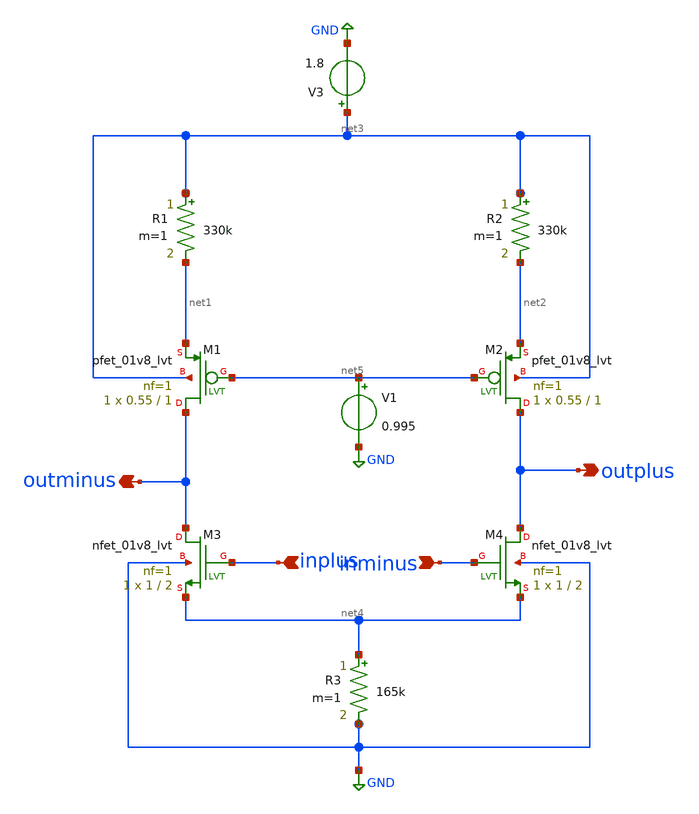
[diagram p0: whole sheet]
** sch_path: botopamp.sch
**.subckt botopamp inplus outminus outplus inminus
*.ipin inplus
*.opin outminus
*.opin outplus
*.ipin inminus
XM1 outminus net5 net1 net3 sky130_fd_pr__pfet_01v8_lvt L=1 W=0.55 nf=1 ad='int((nf+1)/2) * W/nf * 0.29'
+ as='int((nf+2)/2) * W/nf * 0.29' pd='2*int((nf+1)/2) * (W/nf + 0.29)' ps='2*int((nf+2)/2) * (W/nf + 0.29)'
+ nrd='0.29 / W' nrs='0.29 / W' sa=0 sb=0 sd=0 mult=1 m=1
XM2 outplus net5 net2 net3 sky130_fd_pr__pfet_01v8_lvt L=1 W=0.55 nf=1 ad='int((nf+1)/2) * W/nf * 0.29'
+ as='int((nf+2)/2) * W/nf * 0.29' pd='2*int((nf+1)/2) * (W/nf + 0.29)' ps='2*int((nf+2)/2) * (W/nf + 0.29)'
+ nrd='0.29 / W' nrs='0.29 / W' sa=0 sb=0 sd=0 mult=1 m=1
XM3 outminus inplus net4 GND sky130_fd_pr__nfet_01v8_lvt L=2 W=1 nf=1 ad='int((nf+1)/2) * W/nf * 0.29'
+ as='int((nf+2)/2) * W/nf * 0.29' pd='2*int((nf+1)/2) * (W/nf + 0.29)' ps='2*int((nf+2)/2) * (W/nf + 0.29)'
+ nrd='0.29 / W' nrs='0.29 / W' sa=0 sb=0 sd=0 mult=1 m=1
XM4 outplus inminus net4 GND sky130_fd_pr__nfet_01v8_lvt L=2 W=1 nf=1 ad='int((nf+1)/2) * W/nf * 0.29'
+ as='int((nf+2)/2) * W/nf * 0.29' pd='2*int((nf+1)/2) * (W/nf + 0.29)' ps='2*int((nf+2)/2) * (W/nf + 0.29)'
+ nrd='0.29 / W' nrs='0.29 / W' sa=0 sb=0 sd=0 mult=1 m=1
R1 net3 net1 330k m=1
R2 net3 net2 330k m=1
R3 net4 GND 165k m=1
V1 net5 GND 0.995
V3 net3 GND 1.8
**.ends
.GLOBAL GND
.end
